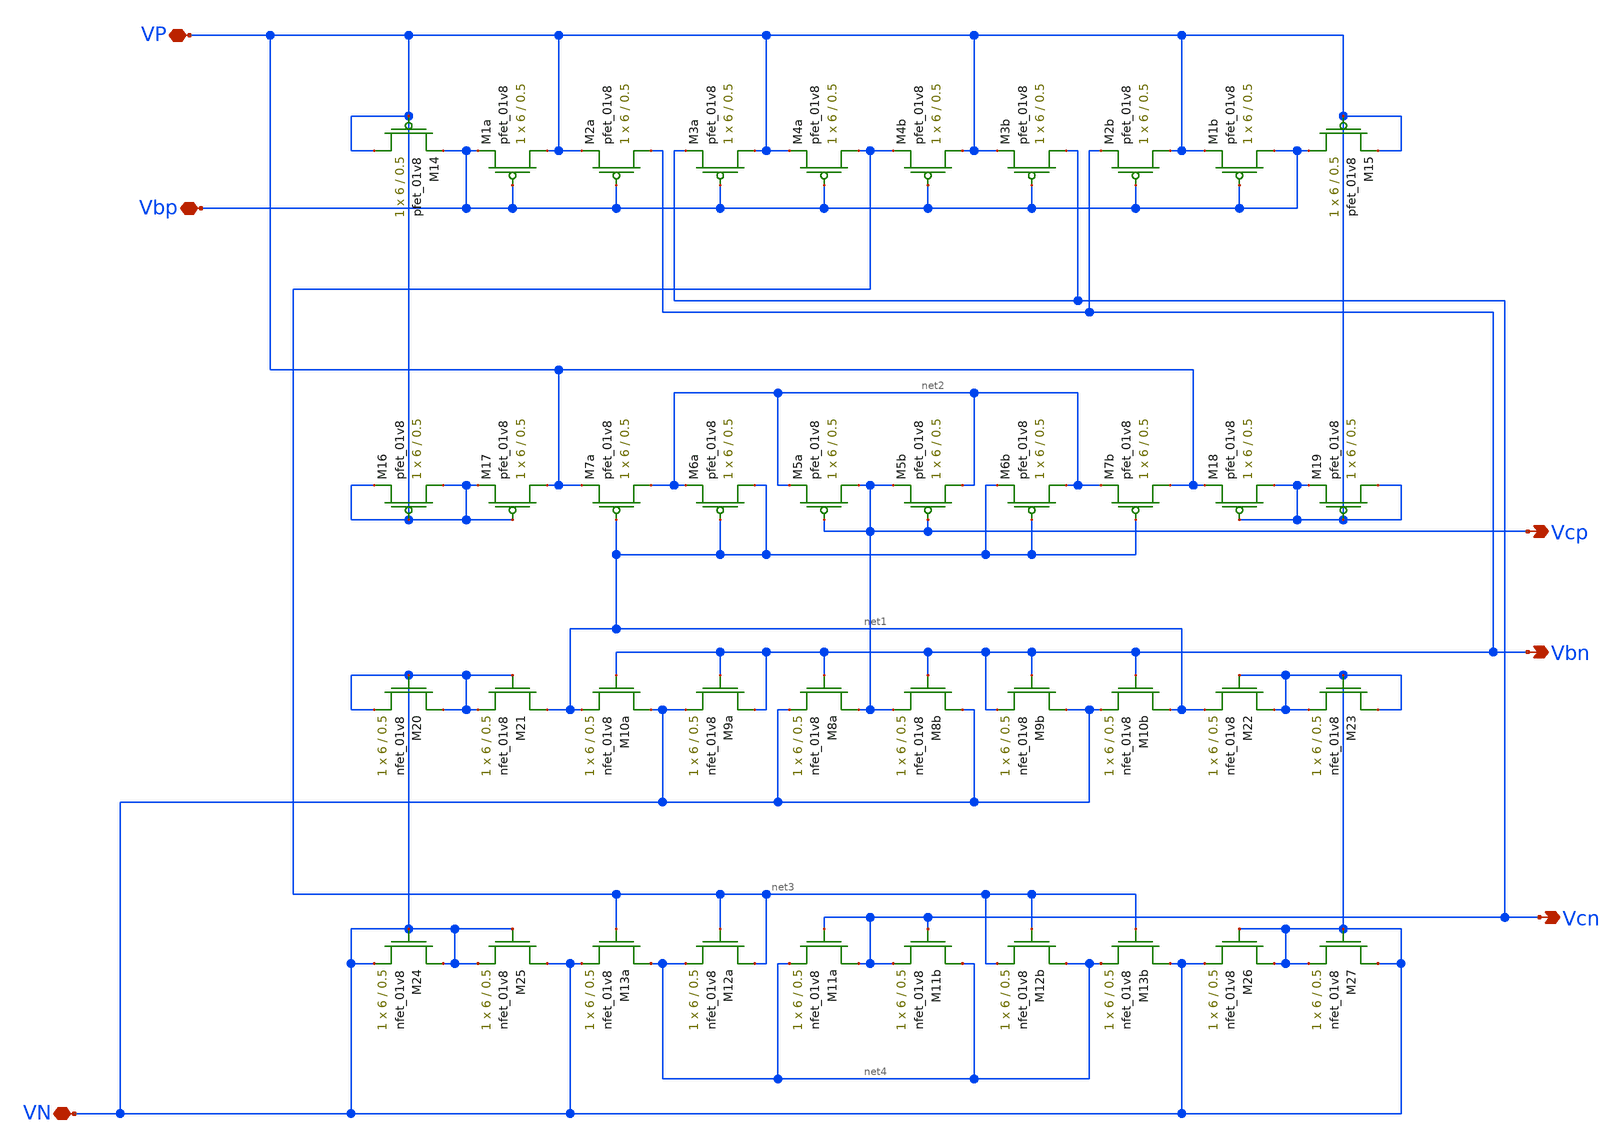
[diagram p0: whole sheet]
** sch_path: MP3/simulations/bias-lds.sch
**.subckt bias-lds VP Vbp Vcp VN Vbn Vcn
*.iopin VP
*.iopin Vbp
*.opin Vcp
*.iopin VN
*.opin Vbn
*.opin Vcn
XM1a VP Vbp Vbp VDD sky130_fd_pr__pfet_01v8 L=0.5 W=6 nf=1 ad='int((nf+1)/2) * W/nf * 0.29' as='int((nf+2)/2) * W/nf * 0.29'
+ pd='2*int((nf+1)/2) * (W/nf + 0.29)' ps='2*int((nf+2)/2) * (W/nf + 0.29)' nrd='0.29 / W' nrs='0.29 / W'
+ sa=0 sb=0 sd=0 mult=1 m=1
XM2a Vbn Vbp VP VDD sky130_fd_pr__pfet_01v8 L=0.5 W=6 nf=1 ad='int((nf+1)/2) * W/nf * 0.29' as='int((nf+2)/2) * W/nf * 0.29'
+ pd='2*int((nf+1)/2) * (W/nf + 0.29)' ps='2*int((nf+2)/2) * (W/nf + 0.29)' nrd='0.29 / W' nrs='0.29 / W'
+ sa=0 sb=0 sd=0 mult=1 m=1
XM3a VP Vbp Vcn VDD sky130_fd_pr__pfet_01v8 L=0.5 W=6 nf=1 ad='int((nf+1)/2) * W/nf * 0.29' as='int((nf+2)/2) * W/nf * 0.29'
+ pd='2*int((nf+1)/2) * (W/nf + 0.29)' ps='2*int((nf+2)/2) * (W/nf + 0.29)' nrd='0.29 / W' nrs='0.29 / W'
+ sa=0 sb=0 sd=0 mult=1 m=1
XM4a net3 Vbp VP VDD sky130_fd_pr__pfet_01v8 L=0.5 W=6 nf=1 ad='int((nf+1)/2) * W/nf * 0.29' as='int((nf+2)/2) * W/nf * 0.29'
+ pd='2*int((nf+1)/2) * (W/nf + 0.29)' ps='2*int((nf+2)/2) * (W/nf + 0.29)' nrd='0.29 / W' nrs='0.29 / W'
+ sa=0 sb=0 sd=0 mult=1 m=1
XM4b VP Vbp net3 VDD sky130_fd_pr__pfet_01v8 L=0.5 W=6 nf=1 ad='int((nf+1)/2) * W/nf * 0.29' as='int((nf+2)/2) * W/nf * 0.29'
+ pd='2*int((nf+1)/2) * (W/nf + 0.29)' ps='2*int((nf+2)/2) * (W/nf + 0.29)' nrd='0.29 / W' nrs='0.29 / W'
+ sa=0 sb=0 sd=0 mult=1 m=1
XM3b Vcn Vbp VP VDD sky130_fd_pr__pfet_01v8 L=0.5 W=6 nf=1 ad='int((nf+1)/2) * W/nf * 0.29' as='int((nf+2)/2) * W/nf * 0.29'
+ pd='2*int((nf+1)/2) * (W/nf + 0.29)' ps='2*int((nf+2)/2) * (W/nf + 0.29)' nrd='0.29 / W' nrs='0.29 / W'
+ sa=0 sb=0 sd=0 mult=1 m=1
XM2b VP Vbp Vbn VDD sky130_fd_pr__pfet_01v8 L=0.5 W=6 nf=1 ad='int((nf+1)/2) * W/nf * 0.29' as='int((nf+2)/2) * W/nf * 0.29'
+ pd='2*int((nf+1)/2) * (W/nf + 0.29)' ps='2*int((nf+2)/2) * (W/nf + 0.29)' nrd='0.29 / W' nrs='0.29 / W'
+ sa=0 sb=0 sd=0 mult=1 m=1
XM1b Vbp Vbp VP VDD sky130_fd_pr__pfet_01v8 L=0.5 W=6 nf=1 ad='int((nf+1)/2) * W/nf * 0.29' as='int((nf+2)/2) * W/nf * 0.29'
+ pd='2*int((nf+1)/2) * (W/nf + 0.29)' ps='2*int((nf+2)/2) * (W/nf + 0.29)' nrd='0.29 / W' nrs='0.29 / W'
+ sa=0 sb=0 sd=0 mult=1 m=1
XM7a net2 net1 VP VDD sky130_fd_pr__pfet_01v8 L=0.5 W=6 nf=1 ad='int((nf+1)/2) * W/nf * 0.29' as='int((nf+2)/2) * W/nf * 0.29'
+ pd='2*int((nf+1)/2) * (W/nf + 0.29)' ps='2*int((nf+2)/2) * (W/nf + 0.29)' nrd='0.29 / W' nrs='0.29 / W'
+ sa=0 sb=0 sd=0 mult=1 m=1
XM6a net1 net1 net2 VDD sky130_fd_pr__pfet_01v8 L=0.5 W=6 nf=1 ad='int((nf+1)/2) * W/nf * 0.29' as='int((nf+2)/2) * W/nf * 0.29'
+ pd='2*int((nf+1)/2) * (W/nf + 0.29)' ps='2*int((nf+2)/2) * (W/nf + 0.29)' nrd='0.29 / W' nrs='0.29 / W'
+ sa=0 sb=0 sd=0 mult=1 m=1
XM5a Vcp Vcp net2 VDD sky130_fd_pr__pfet_01v8 L=0.5 W=6 nf=1 ad='int((nf+1)/2) * W/nf * 0.29' as='int((nf+2)/2) * W/nf * 0.29'
+ pd='2*int((nf+1)/2) * (W/nf + 0.29)' ps='2*int((nf+2)/2) * (W/nf + 0.29)' nrd='0.29 / W' nrs='0.29 / W'
+ sa=0 sb=0 sd=0 mult=1 m=1
XM5b net2 Vcp Vcp VDD sky130_fd_pr__pfet_01v8 L=0.5 W=6 nf=1 ad='int((nf+1)/2) * W/nf * 0.29' as='int((nf+2)/2) * W/nf * 0.29'
+ pd='2*int((nf+1)/2) * (W/nf + 0.29)' ps='2*int((nf+2)/2) * (W/nf + 0.29)' nrd='0.29 / W' nrs='0.29 / W'
+ sa=0 sb=0 sd=0 mult=1 m=1
XM6b net2 net1 net1 VDD sky130_fd_pr__pfet_01v8 L=0.5 W=6 nf=1 ad='int((nf+1)/2) * W/nf * 0.29' as='int((nf+2)/2) * W/nf * 0.29'
+ pd='2*int((nf+1)/2) * (W/nf + 0.29)' ps='2*int((nf+2)/2) * (W/nf + 0.29)' nrd='0.29 / W' nrs='0.29 / W'
+ sa=0 sb=0 sd=0 mult=1 m=1
XM7b VP net1 net2 VDD sky130_fd_pr__pfet_01v8 L=0.5 W=6 nf=1 ad='int((nf+1)/2) * W/nf * 0.29' as='int((nf+2)/2) * W/nf * 0.29'
+ pd='2*int((nf+1)/2) * (W/nf + 0.29)' ps='2*int((nf+2)/2) * (W/nf + 0.29)' nrd='0.29 / W' nrs='0.29 / W'
+ sa=0 sb=0 sd=0 mult=1 m=1
XM10a VN Vbn net1 GND sky130_fd_pr__nfet_01v8 L=0.5 W=6 nf=1 ad='int((nf+1)/2) * W/nf * 0.29' as='int((nf+2)/2) * W/nf * 0.29'
+ pd='2*int((nf+1)/2) * (W/nf + 0.29)' ps='2*int((nf+2)/2) * (W/nf + 0.29)' nrd='0.29 / W' nrs='0.29 / W'
+ sa=0 sb=0 sd=0 mult=1 m=1
XM9a Vbn Vbn VN GND sky130_fd_pr__nfet_01v8 L=0.5 W=6 nf=1 ad='int((nf+1)/2) * W/nf * 0.29' as='int((nf+2)/2) * W/nf * 0.29'
+ pd='2*int((nf+1)/2) * (W/nf + 0.29)' ps='2*int((nf+2)/2) * (W/nf + 0.29)' nrd='0.29 / W' nrs='0.29 / W'
+ sa=0 sb=0 sd=0 mult=1 m=1
XM8a Vcp Vbn VN GND sky130_fd_pr__nfet_01v8 L=0.5 W=6 nf=1 ad='int((nf+1)/2) * W/nf * 0.29' as='int((nf+2)/2) * W/nf * 0.29'
+ pd='2*int((nf+1)/2) * (W/nf + 0.29)' ps='2*int((nf+2)/2) * (W/nf + 0.29)' nrd='0.29 / W' nrs='0.29 / W'
+ sa=0 sb=0 sd=0 mult=1 m=1
XM8b VN Vbn Vcp GND sky130_fd_pr__nfet_01v8 L=0.5 W=6 nf=1 ad='int((nf+1)/2) * W/nf * 0.29' as='int((nf+2)/2) * W/nf * 0.29'
+ pd='2*int((nf+1)/2) * (W/nf + 0.29)' ps='2*int((nf+2)/2) * (W/nf + 0.29)' nrd='0.29 / W' nrs='0.29 / W'
+ sa=0 sb=0 sd=0 mult=1 m=1
XM9b VN Vbn Vbn GND sky130_fd_pr__nfet_01v8 L=0.5 W=6 nf=1 ad='int((nf+1)/2) * W/nf * 0.29' as='int((nf+2)/2) * W/nf * 0.29'
+ pd='2*int((nf+1)/2) * (W/nf + 0.29)' ps='2*int((nf+2)/2) * (W/nf + 0.29)' nrd='0.29 / W' nrs='0.29 / W'
+ sa=0 sb=0 sd=0 mult=1 m=1
XM10b net1 Vbn VN GND sky130_fd_pr__nfet_01v8 L=0.5 W=6 nf=1 ad='int((nf+1)/2) * W/nf * 0.29' as='int((nf+2)/2) * W/nf * 0.29'
+ pd='2*int((nf+1)/2) * (W/nf + 0.29)' ps='2*int((nf+2)/2) * (W/nf + 0.29)' nrd='0.29 / W' nrs='0.29 / W'
+ sa=0 sb=0 sd=0 mult=1 m=1
XM13a net4 net3 VN GND sky130_fd_pr__nfet_01v8 L=0.5 W=6 nf=1 ad='int((nf+1)/2) * W/nf * 0.29' as='int((nf+2)/2) * W/nf * 0.29'
+ pd='2*int((nf+1)/2) * (W/nf + 0.29)' ps='2*int((nf+2)/2) * (W/nf + 0.29)' nrd='0.29 / W' nrs='0.29 / W'
+ sa=0 sb=0 sd=0 mult=1 m=1
XM12a net3 net3 net4 GND sky130_fd_pr__nfet_01v8 L=0.5 W=6 nf=1 ad='int((nf+1)/2) * W/nf * 0.29' as='int((nf+2)/2) * W/nf * 0.29'
+ pd='2*int((nf+1)/2) * (W/nf + 0.29)' ps='2*int((nf+2)/2) * (W/nf + 0.29)' nrd='0.29 / W' nrs='0.29 / W'
+ sa=0 sb=0 sd=0 mult=1 m=1
XM11a Vcn Vcn net4 GND sky130_fd_pr__nfet_01v8 L=0.5 W=6 nf=1 ad='int((nf+1)/2) * W/nf * 0.29' as='int((nf+2)/2) * W/nf * 0.29'
+ pd='2*int((nf+1)/2) * (W/nf + 0.29)' ps='2*int((nf+2)/2) * (W/nf + 0.29)' nrd='0.29 / W' nrs='0.29 / W'
+ sa=0 sb=0 sd=0 mult=1 m=1
XM11b net4 Vcn Vcn GND sky130_fd_pr__nfet_01v8 L=0.5 W=6 nf=1 ad='int((nf+1)/2) * W/nf * 0.29' as='int((nf+2)/2) * W/nf * 0.29'
+ pd='2*int((nf+1)/2) * (W/nf + 0.29)' ps='2*int((nf+2)/2) * (W/nf + 0.29)' nrd='0.29 / W' nrs='0.29 / W'
+ sa=0 sb=0 sd=0 mult=1 m=1
XM12b net4 net3 net3 GND sky130_fd_pr__nfet_01v8 L=0.5 W=6 nf=1 ad='int((nf+1)/2) * W/nf * 0.29' as='int((nf+2)/2) * W/nf * 0.29'
+ pd='2*int((nf+1)/2) * (W/nf + 0.29)' ps='2*int((nf+2)/2) * (W/nf + 0.29)' nrd='0.29 / W' nrs='0.29 / W'
+ sa=0 sb=0 sd=0 mult=1 m=1
XM13b VN net3 net4 GND sky130_fd_pr__nfet_01v8 L=0.5 W=6 nf=1 ad='int((nf+1)/2) * W/nf * 0.29' as='int((nf+2)/2) * W/nf * 0.29'
+ pd='2*int((nf+1)/2) * (W/nf + 0.29)' ps='2*int((nf+2)/2) * (W/nf + 0.29)' nrd='0.29 / W' nrs='0.29 / W'
+ sa=0 sb=0 sd=0 mult=1 m=1
XM15 Vbp VP VP VDD sky130_fd_pr__pfet_01v8 L=0.5 W=6 nf=1 ad='int((nf+1)/2) * W/nf * 0.29' as='int((nf+2)/2) * W/nf * 0.29'
+ pd='2*int((nf+1)/2) * (W/nf + 0.29)' ps='2*int((nf+2)/2) * (W/nf + 0.29)' nrd='0.29 / W' nrs='0.29 / W'
+ sa=0 sb=0 sd=0 mult=1 m=1
XM14 VP VP Vbp VDD sky130_fd_pr__pfet_01v8 L=0.5 W=6 nf=1 ad='int((nf+1)/2) * W/nf * 0.29' as='int((nf+2)/2) * W/nf * 0.29'
+ pd='2*int((nf+1)/2) * (W/nf + 0.29)' ps='2*int((nf+2)/2) * (W/nf + 0.29)' nrd='0.29 / W' nrs='0.29 / W'
+ sa=0 sb=0 sd=0 mult=1 m=1
XM17 VP VP VP VDD sky130_fd_pr__pfet_01v8 L=0.5 W=6 nf=1 ad='int((nf+1)/2) * W/nf * 0.29' as='int((nf+2)/2) * W/nf * 0.29'
+ pd='2*int((nf+1)/2) * (W/nf + 0.29)' ps='2*int((nf+2)/2) * (W/nf + 0.29)' nrd='0.29 / W' nrs='0.29 / W'
+ sa=0 sb=0 sd=0 mult=1 m=1
XM16 VP VP VP VDD sky130_fd_pr__pfet_01v8 L=0.5 W=6 nf=1 ad='int((nf+1)/2) * W/nf * 0.29' as='int((nf+2)/2) * W/nf * 0.29'
+ pd='2*int((nf+1)/2) * (W/nf + 0.29)' ps='2*int((nf+2)/2) * (W/nf + 0.29)' nrd='0.29 / W' nrs='0.29 / W'
+ sa=0 sb=0 sd=0 mult=1 m=1
XM21 net1 VN VN GND sky130_fd_pr__nfet_01v8 L=0.5 W=6 nf=1 ad='int((nf+1)/2) * W/nf * 0.29' as='int((nf+2)/2) * W/nf * 0.29'
+ pd='2*int((nf+1)/2) * (W/nf + 0.29)' ps='2*int((nf+2)/2) * (W/nf + 0.29)' nrd='0.29 / W' nrs='0.29 / W'
+ sa=0 sb=0 sd=0 mult=1 m=1
XM20 VN VN VN GND sky130_fd_pr__nfet_01v8 L=0.5 W=6 nf=1 ad='int((nf+1)/2) * W/nf * 0.29' as='int((nf+2)/2) * W/nf * 0.29'
+ pd='2*int((nf+1)/2) * (W/nf + 0.29)' ps='2*int((nf+2)/2) * (W/nf + 0.29)' nrd='0.29 / W' nrs='0.29 / W'
+ sa=0 sb=0 sd=0 mult=1 m=1
XM25 VN VN VN GND sky130_fd_pr__nfet_01v8 L=0.5 W=6 nf=1 ad='int((nf+1)/2) * W/nf * 0.29' as='int((nf+2)/2) * W/nf * 0.29'
+ pd='2*int((nf+1)/2) * (W/nf + 0.29)' ps='2*int((nf+2)/2) * (W/nf + 0.29)' nrd='0.29 / W' nrs='0.29 / W'
+ sa=0 sb=0 sd=0 mult=1 m=1
XM24 VN VN VN GND sky130_fd_pr__nfet_01v8 L=0.5 W=6 nf=1 ad='int((nf+1)/2) * W/nf * 0.29' as='int((nf+2)/2) * W/nf * 0.29'
+ pd='2*int((nf+1)/2) * (W/nf + 0.29)' ps='2*int((nf+2)/2) * (W/nf + 0.29)' nrd='0.29 / W' nrs='0.29 / W'
+ sa=0 sb=0 sd=0 mult=1 m=1
XM18 VP VP VP VDD sky130_fd_pr__pfet_01v8 L=0.5 W=6 nf=1 ad='int((nf+1)/2) * W/nf * 0.29' as='int((nf+2)/2) * W/nf * 0.29'
+ pd='2*int((nf+1)/2) * (W/nf + 0.29)' ps='2*int((nf+2)/2) * (W/nf + 0.29)' nrd='0.29 / W' nrs='0.29 / W'
+ sa=0 sb=0 sd=0 mult=1 m=1
XM19 VP VP VP VDD sky130_fd_pr__pfet_01v8 L=0.5 W=6 nf=1 ad='int((nf+1)/2) * W/nf * 0.29' as='int((nf+2)/2) * W/nf * 0.29'
+ pd='2*int((nf+1)/2) * (W/nf + 0.29)' ps='2*int((nf+2)/2) * (W/nf + 0.29)' nrd='0.29 / W' nrs='0.29 / W'
+ sa=0 sb=0 sd=0 mult=1 m=1
XM22 VN VN net1 GND sky130_fd_pr__nfet_01v8 L=0.5 W=6 nf=1 ad='int((nf+1)/2) * W/nf * 0.29' as='int((nf+2)/2) * W/nf * 0.29'
+ pd='2*int((nf+1)/2) * (W/nf + 0.29)' ps='2*int((nf+2)/2) * (W/nf + 0.29)' nrd='0.29 / W' nrs='0.29 / W'
+ sa=0 sb=0 sd=0 mult=1 m=1
XM23 VN VN VN GND sky130_fd_pr__nfet_01v8 L=0.5 W=6 nf=1 ad='int((nf+1)/2) * W/nf * 0.29' as='int((nf+2)/2) * W/nf * 0.29'
+ pd='2*int((nf+1)/2) * (W/nf + 0.29)' ps='2*int((nf+2)/2) * (W/nf + 0.29)' nrd='0.29 / W' nrs='0.29 / W'
+ sa=0 sb=0 sd=0 mult=1 m=1
XM26 VN VN VN GND sky130_fd_pr__nfet_01v8 L=0.5 W=6 nf=1 ad='int((nf+1)/2) * W/nf * 0.29' as='int((nf+2)/2) * W/nf * 0.29'
+ pd='2*int((nf+1)/2) * (W/nf + 0.29)' ps='2*int((nf+2)/2) * (W/nf + 0.29)' nrd='0.29 / W' nrs='0.29 / W'
+ sa=0 sb=0 sd=0 mult=1 m=1
XM27 VN VN VN GND sky130_fd_pr__nfet_01v8 L=0.5 W=6 nf=1 ad='int((nf+1)/2) * W/nf * 0.29' as='int((nf+2)/2) * W/nf * 0.29'
+ pd='2*int((nf+1)/2) * (W/nf + 0.29)' ps='2*int((nf+2)/2) * (W/nf + 0.29)' nrd='0.29 / W' nrs='0.29 / W'
+ sa=0 sb=0 sd=0 mult=1 m=1
**.ends
.end
